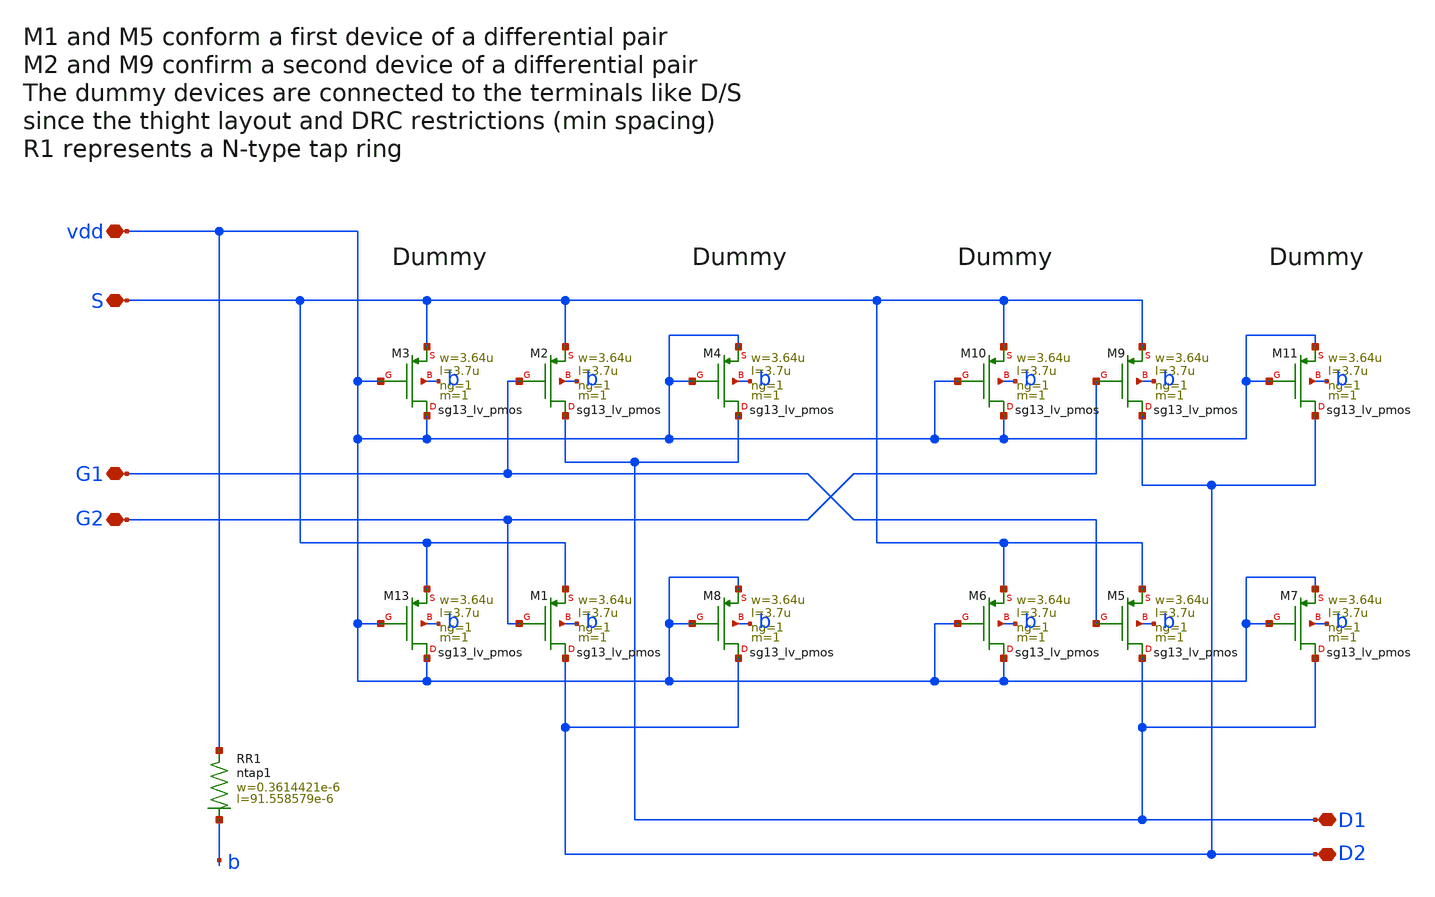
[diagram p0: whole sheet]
** sch_path: tests/data/OTA1336/schematic/xschem/payload/diff_pair.sch
**.subckt diff_pair D1 D2 vdd S G1 G2
*.iopin D1
*.iopin D2
*.iopin vdd
*.iopin S
*.iopin G1
*.iopin G2
XM1 D2 G2 S b sg13_lv_pmos w=3.64u l=3.7u ng=1 m=1 mm_ok=0
XM13 vdd vdd S b sg13_lv_pmos w=3.64u l=3.7u ng=1 m=1 mm_ok=0
XR1 vdd b ntap1 R=4.518 w=0.3614421e-6 l=91.558579e-6
XM8 D2 vdd vdd b sg13_lv_pmos w=3.64u l=3.7u ng=1 m=1 mm_ok=0
XM2 D1 G1 S b sg13_lv_pmos w=3.64u l=3.7u ng=1 m=1 mm_ok=0
XM3 vdd vdd S b sg13_lv_pmos w=3.64u l=3.7u ng=1 m=1 mm_ok=0
XM4 D1 vdd vdd b sg13_lv_pmos w=3.64u l=3.7u ng=1 m=1 mm_ok=0
XM5 D1 G1 S b sg13_lv_pmos w=3.64u l=3.7u ng=1 m=1 mm_ok=0
XM6 vdd vdd S b sg13_lv_pmos w=3.64u l=3.7u ng=1 m=1 mm_ok=0
XM7 D1 vdd vdd b sg13_lv_pmos w=3.64u l=3.7u ng=1 m=1 mm_ok=0
XM9 D2 G2 S b sg13_lv_pmos w=3.64u l=3.7u ng=1 m=1 mm_ok=0
XM10 vdd vdd S b sg13_lv_pmos w=3.64u l=3.7u ng=1 m=1 mm_ok=0
XM11 D2 vdd vdd b sg13_lv_pmos w=3.64u l=3.7u ng=1 m=1 mm_ok=0
**.ends
.end
